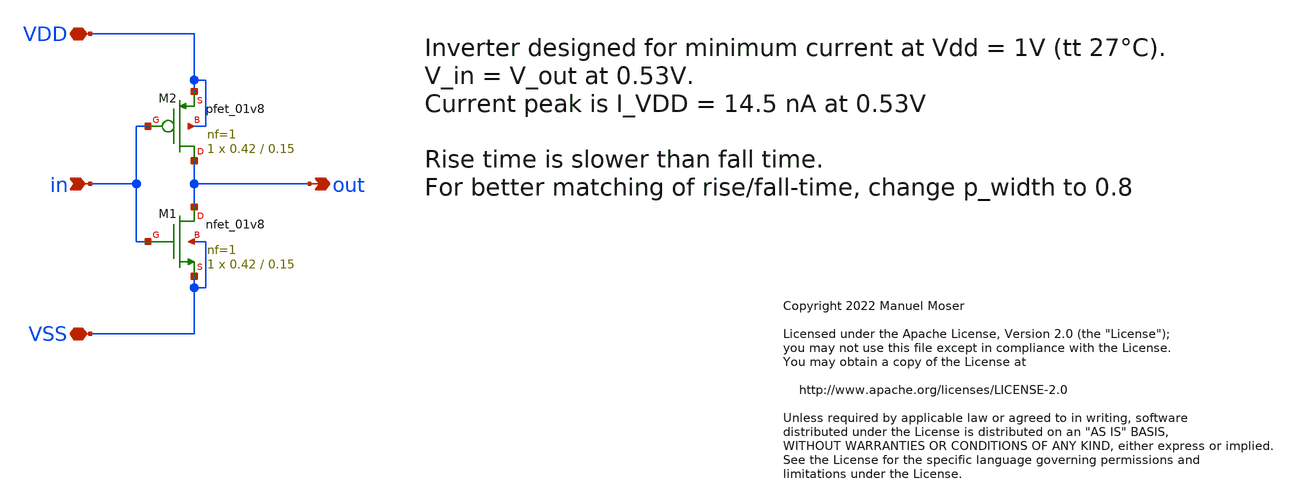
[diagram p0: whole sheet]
** sch_path: xschem/inverter/inverter.sch
* Copyright 2022 Manuel Moser
* Licensed under the Apache License, Version 2.0 (the "License");
**.subckt inverter VDD VSS out in
*.iopin VDD
*.iopin VSS
*.opin out
*.ipin in
XM1 out in VSS VSS sky130_fd_pr__nfet_01v8 L=0.15 W=0.42 nf=1 ad='int((nf+1)/2) * W/nf * 0.29' as='int((nf+2)/2) * W/nf * 0.29'
+ pd='2*int((nf+1)/2) * (W/nf + 0.29)' ps='2*int((nf+2)/2) * (W/nf + 0.29)' nrd='0.29 / W' nrs='0.29 / W'
+ sa=0 sb=0 sd=0 mult=1 m=1
XM2 out in VDD VDD sky130_fd_pr__pfet_01v8 L=0.15 W=0.42 nf=1 ad='int((nf+1)/2) * W/nf * 0.29' as='int((nf+2)/2) * W/nf * 0.29'
+ pd='2*int((nf+1)/2) * (W/nf + 0.29)' ps='2*int((nf+2)/2) * (W/nf + 0.29)' nrd='0.29 / W' nrs='0.29 / W'
+ sa=0 sb=0 sd=0 mult=1 m=1
**.ends
.end
